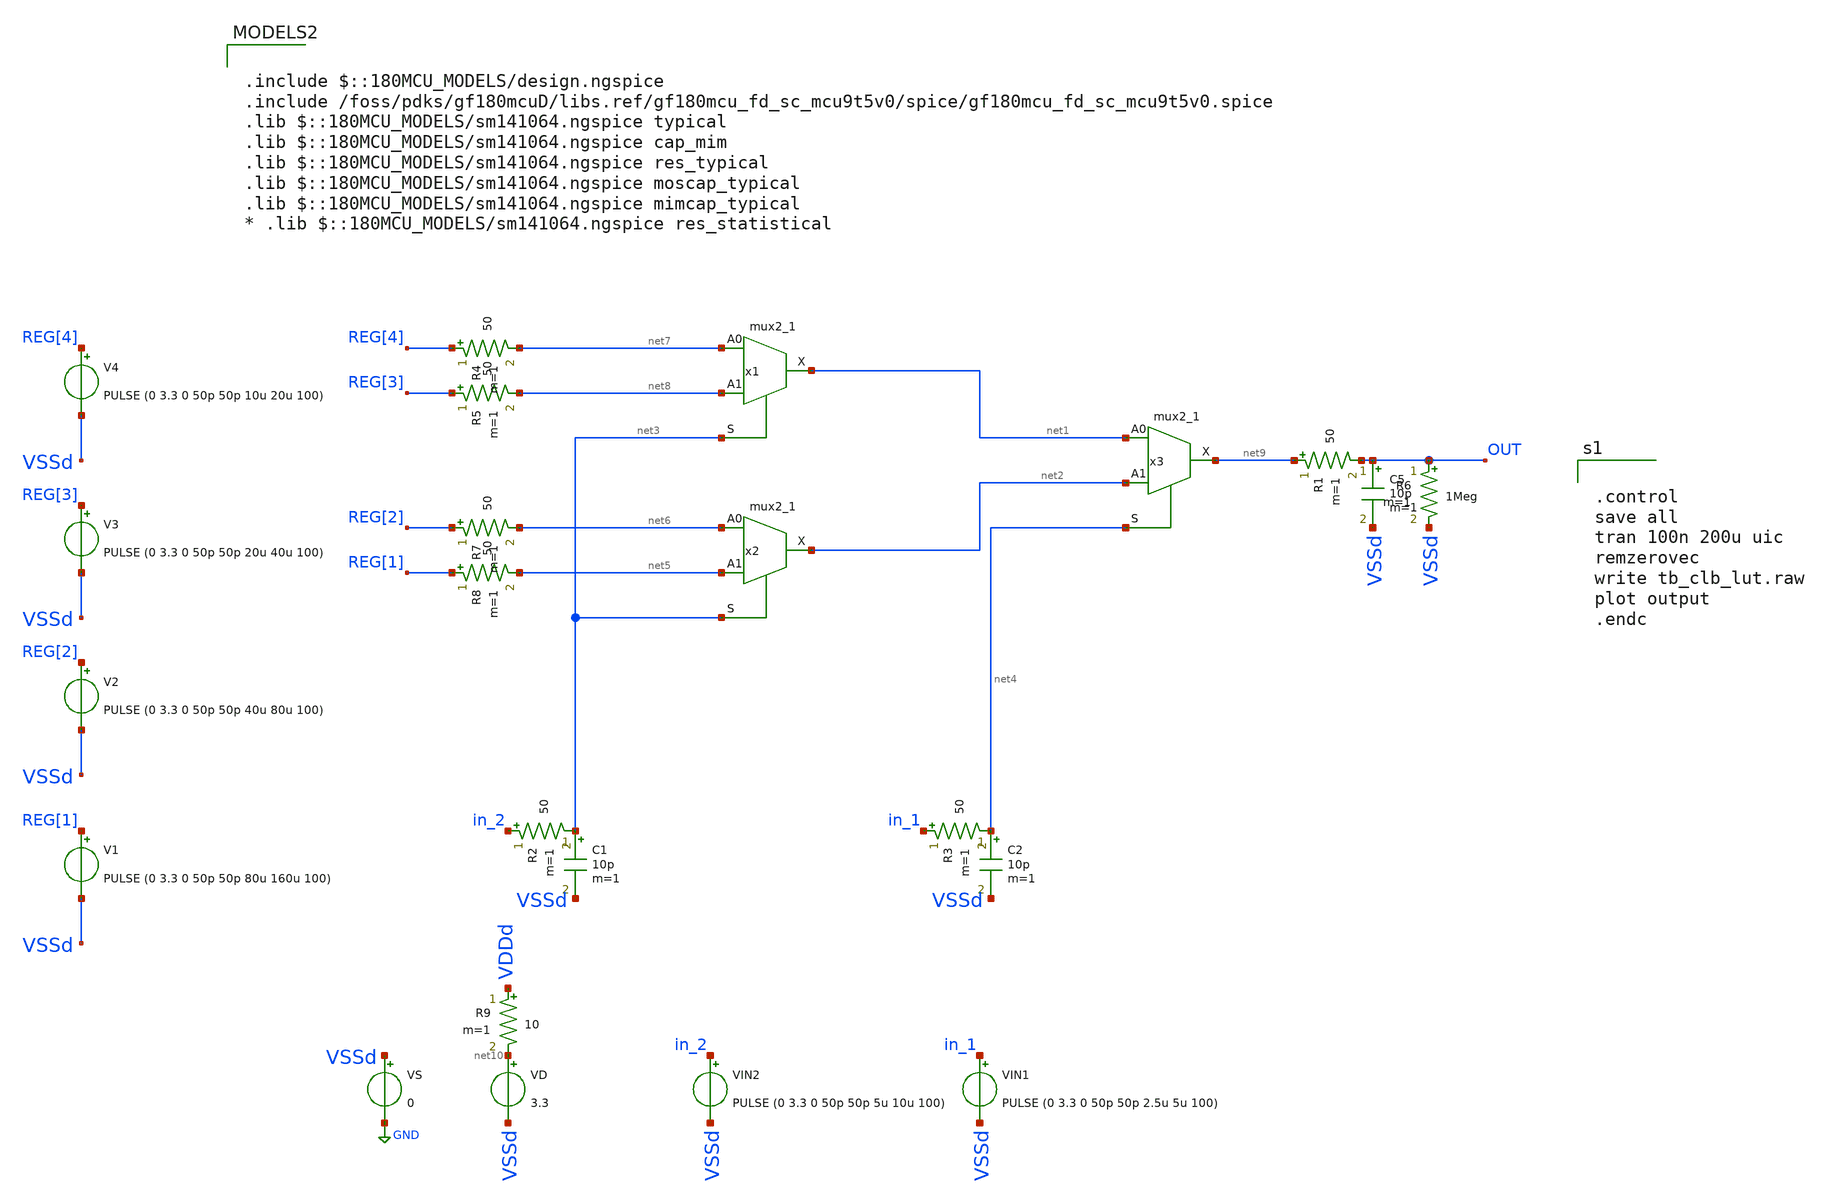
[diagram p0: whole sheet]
** sch_path: designs/libs/tb_fpga/tb_clb/tb_clb_lut.sch
**.subckt tb_clb_lut
x1 net7 net8 net3 VSSd VDDd VSSd VDDd net1 gf180mcu_fd_sc_mcu9t5v0__mux2_1
VIN1 in_1 VSSd PULSE (0 3.3 0 50p 50p 2.5u 5u 100)
VIN2 in_2 VSSd PULSE (0 3.3 0 50p 50p 5u 10u 100)
VD net10 VSSd 3.3
V4 REG[4] VSSd PULSE (0 3.3 0 50p 50p 10u 20u 100)
V3 REG[3] VSSd PULSE (0 3.3 0 50p 50p 20u 40u 100)
V2 REG[2] VSSd PULSE (0 3.3 0 50p 50p 40u 80u 100)
V1 REG[1] VSSd PULSE (0 3.3 0 50p 50p 80u 160u 100)
C5 OUT VSSd 10p m=1
R1 net9 OUT 50 m=1
R6 OUT VSSd 1Meg m=1
C1 net3 VSSd 10p m=1
R2 in_2 net3 50 m=1
C2 net4 VSSd 10p m=1
R3 in_1 net4 50 m=1
R4 REG[4] net7 50 m=1
R5 REG[3] net8 50 m=1
R7 REG[2] net6 50 m=1
R8 REG[1] net5 50 m=1
R9 VDDd net10 10 m=1
VS VSSd GND 0
x2 net6 net5 net3 VSSd VDDd VSSd VDDd net2 gf180mcu_fd_sc_mcu9t5v0__mux2_1
x3 net1 net2 net4 VSSd VDDd VSSd VDDd net9 gf180mcu_fd_sc_mcu9t5v0__mux2_1
**** begin user architecture code


.control
save all
tran 100n 200u uic
remzerovec
write tb_clb_lut.raw
plot output
.endc



.include $::180MCU_MODELS/design.ngspice
.include /foss/pdks/gf180mcuD/libs.ref/gf180mcu_fd_sc_mcu9t5v0/spice/gf180mcu_fd_sc_mcu9t5v0.spice
.lib $::180MCU_MODELS/sm141064.ngspice typical
.lib $::180MCU_MODELS/sm141064.ngspice cap_mim
.lib $::180MCU_MODELS/sm141064.ngspice res_typical
.lib $::180MCU_MODELS/sm141064.ngspice moscap_typical
.lib $::180MCU_MODELS/sm141064.ngspice mimcap_typical
* .lib $::180MCU_MODELS/sm141064.ngspice res_statistical

**** end user architecture code
**.ends
.GLOBAL GND
.end
